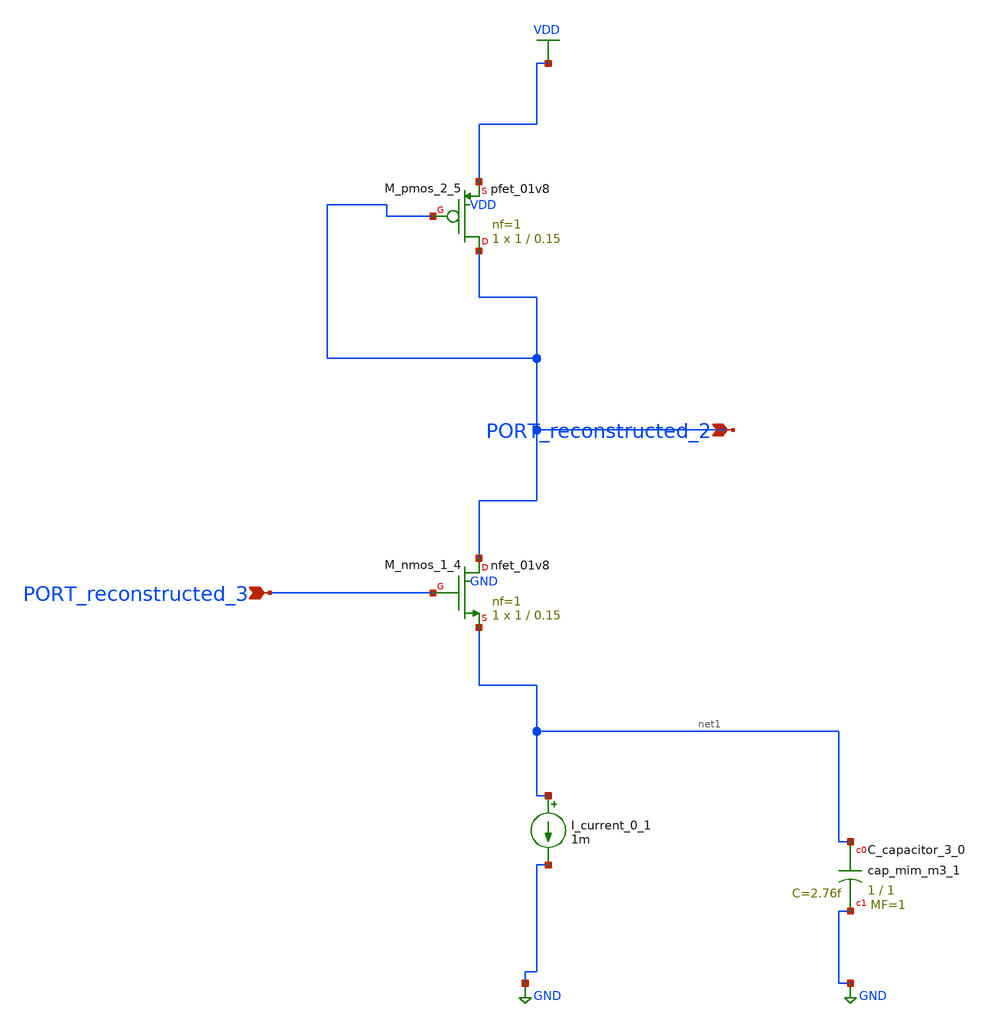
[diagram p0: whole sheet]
** sch_path: schematics/AMSNet/110.sch
**.subckt 110 PORT_reconstructed_2 PORT_reconstructed_3
*.ipin PORT_reconstructed_2
*.ipin PORT_reconstructed_3
XC_capacitor_3_0 net1 GND sky130_fd_pr__cap_mim_m3_1 W=1 L=1 MF=1 m=1
I_current_0_1 net1 GND 1m
XM_nmos_1_4 PORT_reconstructed_2 PORT_reconstructed_3 net1 GND sky130_fd_pr__nfet_01v8 L=0.15 W=1 nf=1
+ ad='int((1 + 1)/2) * 1 / 1 * 0.29' as='int((1 + 2)/2) * 1 / 1 * 0.29' pd='2*int((1 + 1)/2) * (1 / 1 + 0.29)'
+ ps='2*int((1 + 2)/2) * (1 / 1 + 0.29)' nrd='0.29 / 1 ' nrs='0.29 / 1 ' sa=0 sb=0 sd=0 mult=1 m=1
XM_pmos_2_5 PORT_reconstructed_2 PORT_reconstructed_2 VDD VDD sky130_fd_pr__pfet_01v8 L=0.15 W=1 nf=1
+ ad='int((1 + 1)/2) * 1 / 1 * 0.29' as='int((1 + 2)/2) * 1 / 1 * 0.29' pd='2*int((1 + 1)/2) * (1 / 1 + 0.29)'
+ ps='2*int((1 + 2)/2) * (1 / 1 + 0.29)' nrd='0.29 / 1 ' nrs='0.29 / 1 ' sa=0 sb=0 sd=0 mult=1 m=1
**.ends
.GLOBAL GND
.GLOBAL VDD
.end
